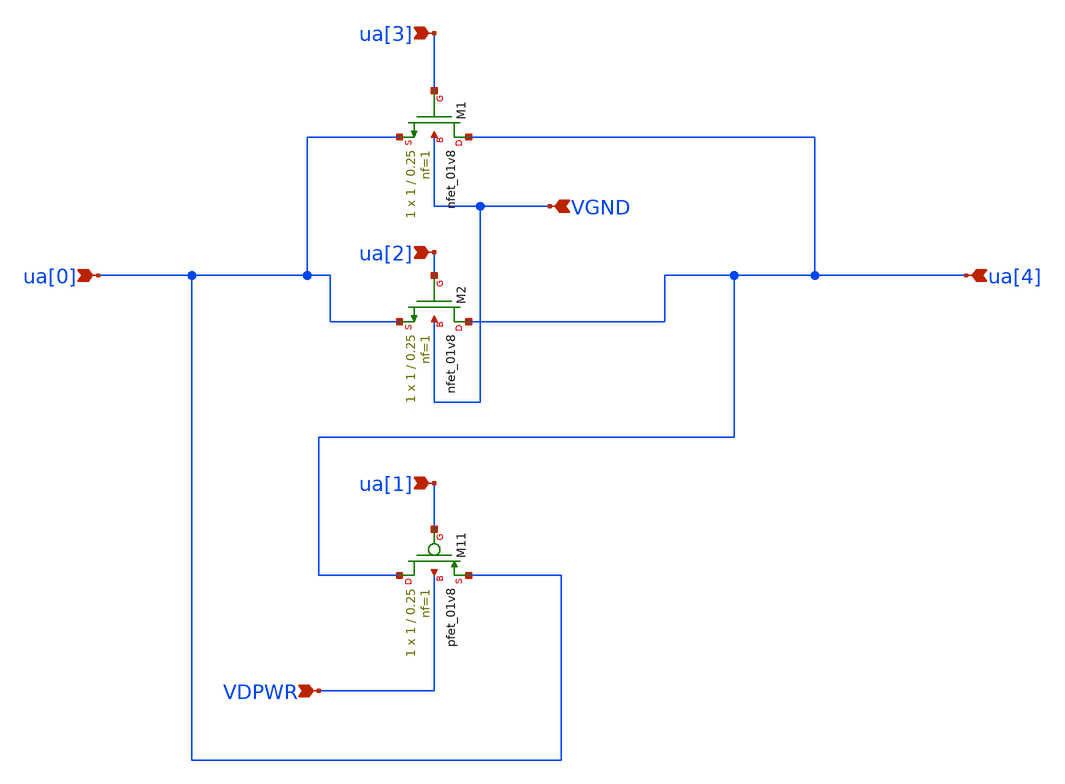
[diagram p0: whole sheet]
** sch_path: custom_gds/tt_um_wakki_0123_Raw_Transistors/mag/tt_um_wakki-0123_Raw_Transistors.sch
**.subckt tt_um_wakki-0123_Raw_Transistors ua[0] ua[1] ua[2] ua[3] ua[4] VDPWR VGND
*.ipin ua[0]
*.ipin ua[1]
*.ipin ua[2]
*.ipin ua[3]
*.ipin ua[4]
*.ipin VDPWR
*.ipin VGND
XM11 ua[4] ua[1] ua[0] VDPWR sky130_fd_pr__pfet_01v8 L=0.25 W=1 nf=1 ad='int((nf+1)/2) * W/nf * 0.29'
+ as='int((nf+2)/2) * W/nf * 0.29' pd='2*int((nf+1)/2) * (W/nf + 0.29)' ps='2*int((nf+2)/2) * (W/nf + 0.29)'
+ nrd='0.29 / W' nrs='0.29 / W' sa=0 sb=0 sd=0 mult=1 m=1
XM2 ua[4] ua[2] ua[0] VGND sky130_fd_pr__nfet_01v8 L=0.25 W=1 nf=1 ad='int((1 + 1)/2) * 1 / 1 * 0.29'
+ as='int((1 + 2)/2) * 1 / 1 * 0.29' pd='2*int((1 + 1)/2) * (1 / 1 + 0.29)' ps='2*int((1 + 2)/2) * (1 / 1 + 0.29)'
+ nrd='0.29 / 1 ' nrs='0.29 / 1 ' sa=0 sb=0 sd=0 mult=1 m=1
XM1 ua[4] ua[3] ua[0] VGND sky130_fd_pr__nfet_01v8 L=0.25 W=1 nf=1 ad='int((1 + 1)/2) * 1 / 1 * 0.29'
+ as='int((1 + 2)/2) * 1 / 1 * 0.29' pd='2*int((1 + 1)/2) * (1 / 1 + 0.29)' ps='2*int((1 + 2)/2) * (1 / 1 + 0.29)'
+ nrd='0.29 / 1 ' nrs='0.29 / 1 ' sa=0 sb=0 sd=0 mult=1 m=1
**.ends
.end
